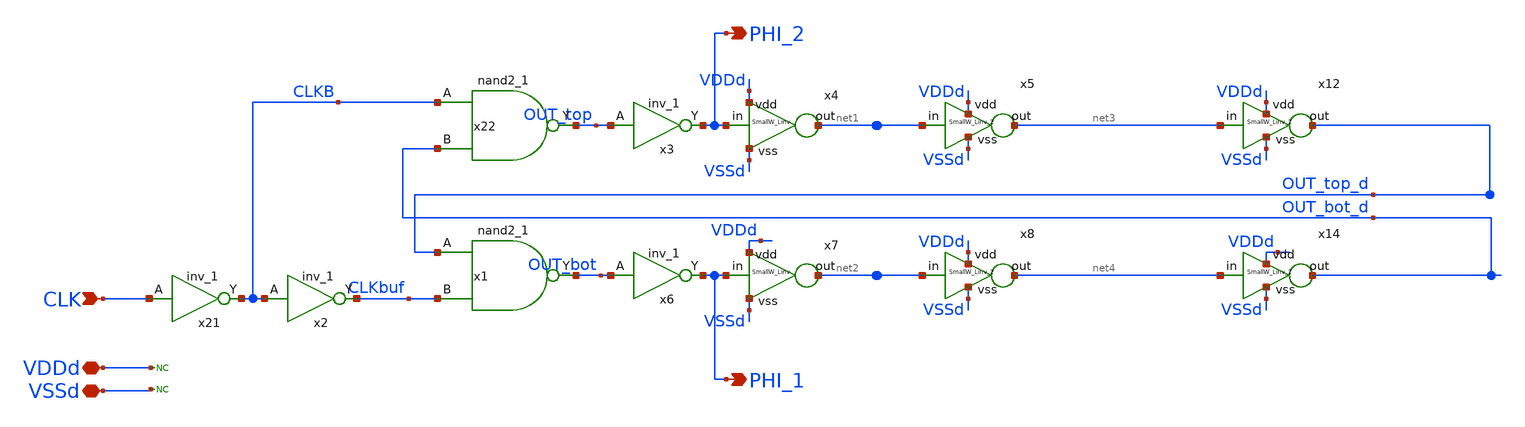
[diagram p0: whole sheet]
** sch_path: designs/libs/qw_core_analog/NOLclk/NOLclk.sch
**.subckt NOLclk CLK PHI_2 VDDd VSSd PHI_1
*.ipin CLK
*.opin PHI_2
*.iopin VDDd
*.iopin VSSd
*.opin PHI_1
* noconn VDDd
* noconn VSSd
x21 CLK VSSd VDDd VSSd VDDd CLKB gf180mcu_fd_sc_mcu9t5v0__inv_1
x22 CLKB OUT_bot_d VSSd VDDd VSSd VDDd OUT_top gf180mcu_fd_sc_mcu9t5v0__nand2_1
x1 OUT_top_d CLKbuf VSSd VDDd VSSd VDDd OUT_bot gf180mcu_fd_sc_mcu9t5v0__nand2_1
x2 CLKB VSSd VDDd VSSd VDDd CLKbuf gf180mcu_fd_sc_mcu9t5v0__inv_1
x6 OUT_bot VSSd VDDd VSSd VDDd PHI_1 gf180mcu_fd_sc_mcu9t5v0__inv_1
x3 OUT_top VSSd VDDd VSSd VDDd PHI_2 gf180mcu_fd_sc_mcu9t5v0__inv_1
x4 VDDd PHI_2 net1 VSSd SmallW_Linv
x7 VDDd PHI_1 net2 VSSd SmallW_Linv
x12 VDDd net3 OUT_top_d VSSd SmallW_Linv_2
x14 VDDd net4 OUT_bot_d VSSd SmallW_Linv_2
x5 VDDd net1 net3 VSSd SmallW_Linv_2
x8 VDDd net2 net4 VSSd SmallW_Linv_2
**.ends

* expanding   symbol:  libs/qw_core_analog/SmallW_Linv/SmallW_Linv.sym # of pins=4
** sym_path: designs/libs/qw_core_analog/SmallW_Linv/SmallW_Linv.sym
** sch_path: designs/libs/qw_core_analog/SmallW_Linv/SmallW_Linv.sch
.subckt SmallW_Linv vdd in out vss
*.iopin in
*.iopin out
*.iopin vdd
*.iopin vss
XM1 out in vss vss nfet_03v3 L=2u W=0.5u nf=1 ad='int((nf+1)/2) * W/nf * 0.18u' as='int((nf+2)/2) * W/nf * 0.18u'
+ pd='2*int((nf+1)/2) * (W/nf + 0.18u)' ps='2*int((nf+2)/2) * (W/nf + 0.18u)' nrd='0.18u / W' nrs='0.18u / W'
+ sa=0 sb=0 sd=0 m=1
XM2 out in vdd vdd pfet_03v3 L=2u W=1u nf=1 ad='int((nf+1)/2) * W/nf * 0.18u' as='int((nf+2)/2) * W/nf * 0.18u'
+ pd='2*int((nf+1)/2) * (W/nf + 0.18u)' ps='2*int((nf+2)/2) * (W/nf + 0.18u)' nrd='0.18u / W' nrs='0.18u / W'
+ sa=0 sb=0 sd=0 m=1
.ends


* expanding   symbol:  libs/qw_core_analog/SmallW_Linv_2/SmallW_Linv_2.sym # of pins=4
** sym_path: designs/libs/qw_core_analog/SmallW_Linv_2/SmallW_Linv_2.sym
** sch_path: designs/libs/qw_core_analog/SmallW_Linv_2/SmallW_Linv_2.sch
.subckt SmallW_Linv_2 vdd in out vss
*.iopin in
*.iopin out
*.iopin vdd
*.iopin vss
XM1 out in vss vss nfet_03v3 L=4u W=0.5u nf=1 ad='int((nf+1)/2) * W/nf * 0.18u' as='int((nf+2)/2) * W/nf * 0.18u'
+ pd='2*int((nf+1)/2) * (W/nf + 0.18u)' ps='2*int((nf+2)/2) * (W/nf + 0.18u)' nrd='0.18u / W' nrs='0.18u / W'
+ sa=0 sb=0 sd=0 m=1
XM2 out in vdd vdd pfet_03v3 L=4u W=1u nf=1 ad='int((nf+1)/2) * W/nf * 0.18u' as='int((nf+2)/2) * W/nf * 0.18u'
+ pd='2*int((nf+1)/2) * (W/nf + 0.18u)' ps='2*int((nf+2)/2) * (W/nf + 0.18u)' nrd='0.18u / W' nrs='0.18u / W'
+ sa=0 sb=0 sd=0 m=1
.ends

.end
